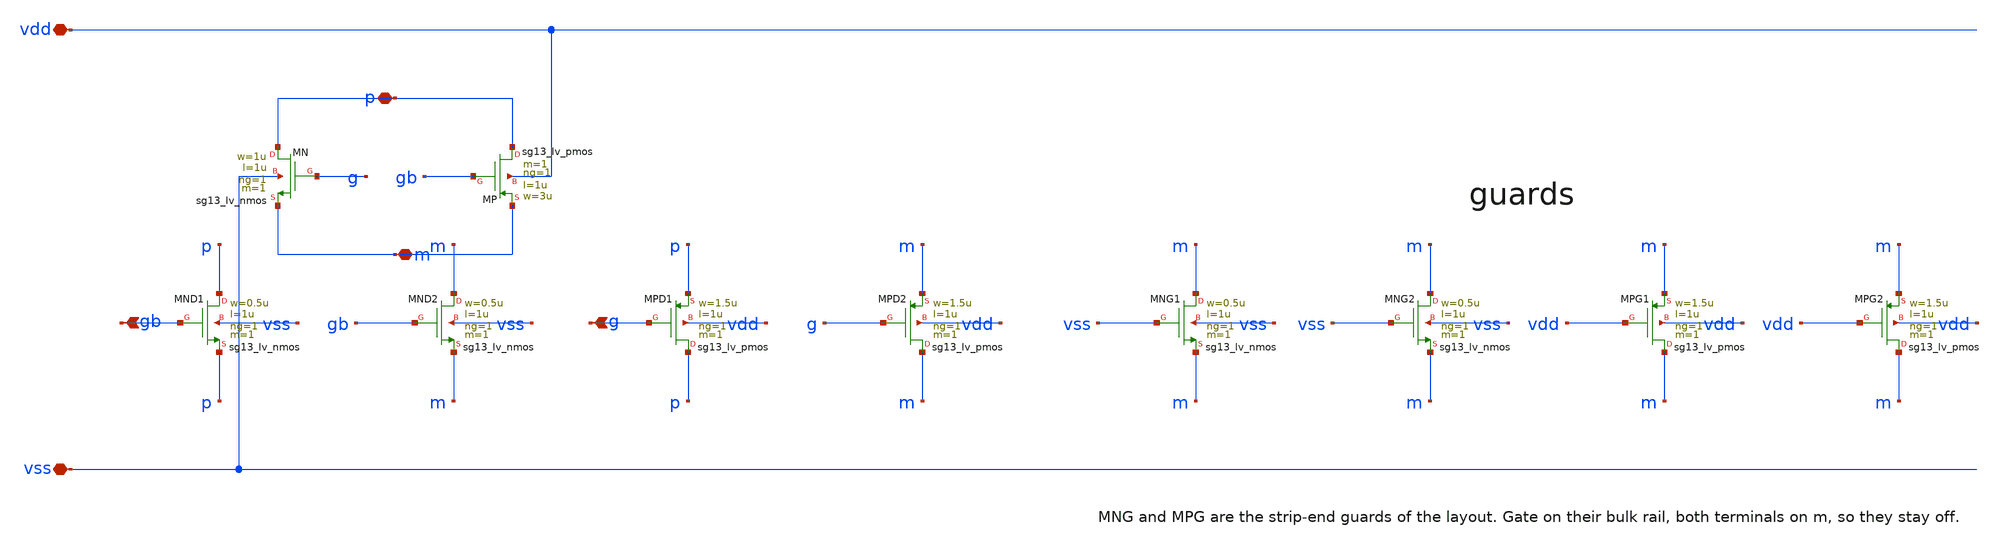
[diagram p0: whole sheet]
** sch_path: ip/dsm2_core/schematic/sw_tgate_cmfb2.sch
**.subckt sw_tgate_cmfb2 vdd vss p m gb g
*.iopin vdd
*.iopin vss
*.iopin p
*.iopin m
*.ipin gb
*.ipin g
XMN p g m vss sg13_lv_nmos w=1u l=1u ng=1 m=1 mm_ok=1
XMP p gb m vdd sg13_lv_pmos w=3u l=1u ng=1 m=1 mm_ok=1
XMND1 p gb p vss sg13_lv_nmos w=0.5u l=1u ng=1 m=1 mm_ok=1
XMND2 m gb m vss sg13_lv_nmos w=0.5u l=1u ng=1 m=1 mm_ok=1
XMPD1 p g p vdd sg13_lv_pmos w=1.5u l=1u ng=1 m=1 mm_ok=1
XMPD2 m g m vdd sg13_lv_pmos w=1.5u l=1u ng=1 m=1 mm_ok=1
XMNG1 m vss m vss sg13_lv_nmos w=0.5u l=1u ng=1 m=1 mm_ok=1
XMNG2 m vss m vss sg13_lv_nmos w=0.5u l=1u ng=1 m=1 mm_ok=1
XMPG1 m vdd m vdd sg13_lv_pmos w=1.5u l=1u ng=1 m=1 mm_ok=1
XMPG2 m vdd m vdd sg13_lv_pmos w=1.5u l=1u ng=1 m=1 mm_ok=1
**.ends
.end
